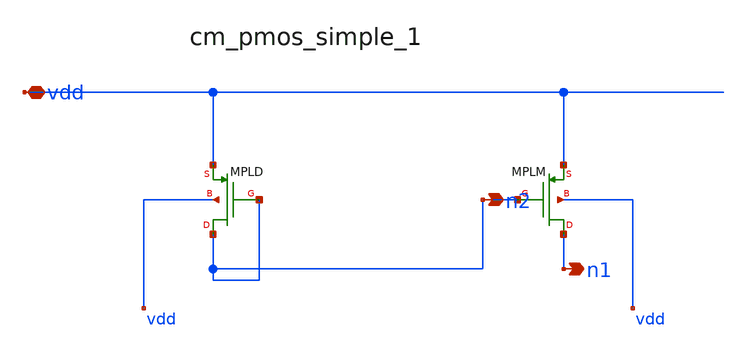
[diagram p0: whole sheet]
** sch_path: analog-db/raw/cmp_001_hyst_diffpair/hier/blocks/cm_pmos_simple_1.sch
**.subckt cm_pmos_simple_1 vdd n2 n1
*.iopin vdd
*.opin n2
*.opin n1
XMPLD n2 n2 vdd vdd sg13_lv_pmos w=x_dut_xmpld_w l=x_dut_xmpld_l ng=1 m=x_dut_xmpld_m
XMPLM n1 n2 vdd vdd sg13_lv_pmos w=x_dut_xmplm_w l=x_dut_xmplm_l ng=1 m=x_dut_xmplm_m
**.ends
.end
